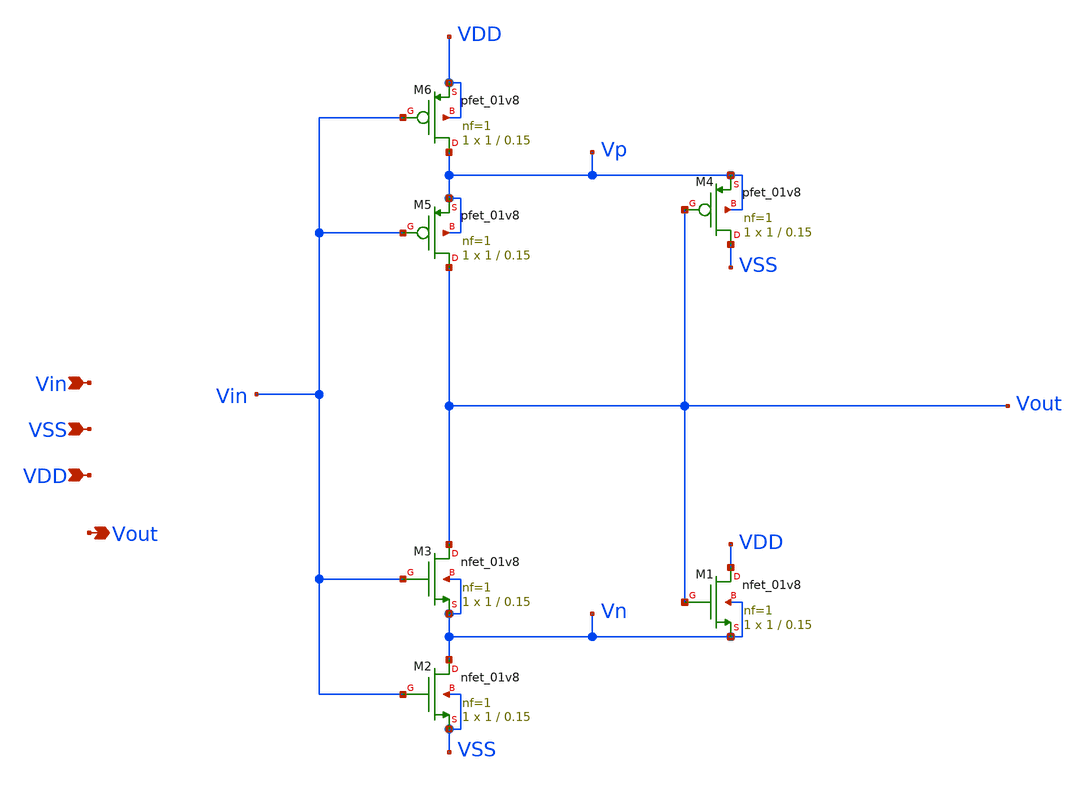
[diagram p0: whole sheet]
** sch_path: xschem/T1/schmTrigg/schmTrigg.sch
**.subckt schmTrigg Vin VDD VSS Vout
*.ipin Vin
*.ipin VDD
*.ipin VSS
*.opin Vout
XM1 VDD Vout Vn Vn sky130_fd_pr__nfet_01v8 L=0.15 W=1 nf=1 ad='int((1 + 1)/2) * 1 / 1 * 0.29' as='int((1 + 2)/2) * 1 / 1 * 0.29'
+ pd='2*int((1 + 1)/2) * (1 / 1 + 0.29)' ps='2*int((1 + 2)/2) * (1 / 1 + 0.29)' nrd='0.29 / 1 ' nrs='0.29 / 1 '
+ sa=0 sb=0 sd=0 mult=1 m=1
XM2 Vn Vin VSS VSS sky130_fd_pr__nfet_01v8 L=0.15 W=1 nf=1 ad='int((1 + 1)/2) * 1 / 1 * 0.29' as='int((1 + 2)/2) * 1 / 1 * 0.29'
+ pd='2*int((1 + 1)/2) * (1 / 1 + 0.29)' ps='2*int((1 + 2)/2) * (1 / 1 + 0.29)' nrd='0.29 / 1 ' nrs='0.29 / 1 '
+ sa=0 sb=0 sd=0 mult=1 m=1
XM3 Vout Vin Vn Vn sky130_fd_pr__nfet_01v8 L=0.15 W=1 nf=1 ad='int((1 + 1)/2) * 1 / 1 * 0.29' as='int((1 + 2)/2) * 1 / 1 * 0.29'
+ pd='2*int((1 + 1)/2) * (1 / 1 + 0.29)' ps='2*int((1 + 2)/2) * (1 / 1 + 0.29)' nrd='0.29 / 1 ' nrs='0.29 / 1 '
+ sa=0 sb=0 sd=0 mult=1 m=1
XM4 VSS Vout Vp Vp sky130_fd_pr__pfet_01v8 L=0.15 W=1 nf=1 ad='int((nf+1)/2) * W/nf * 0.29' as='int((nf+2)/2) * W/nf * 0.29'
+ pd='2*int((nf+1)/2) * (W/nf + 0.29)' ps='2*int((nf+2)/2) * (W/nf + 0.29)' nrd='0.29 / W' nrs='0.29 / W'
+ sa=0 sb=0 sd=0 mult=1 m=1
XM5 Vout Vin Vp Vp sky130_fd_pr__pfet_01v8 L=0.15 W=1 nf=1 ad='int((nf+1)/2) * W/nf * 0.29' as='int((nf+2)/2) * W/nf * 0.29'
+ pd='2*int((nf+1)/2) * (W/nf + 0.29)' ps='2*int((nf+2)/2) * (W/nf + 0.29)' nrd='0.29 / W' nrs='0.29 / W'
+ sa=0 sb=0 sd=0 mult=1 m=1
XM6 Vp Vin VDD VDD sky130_fd_pr__pfet_01v8 L=0.15 W=1 nf=1 ad='int((nf+1)/2) * W/nf * 0.29' as='int((nf+2)/2) * W/nf * 0.29'
+ pd='2*int((nf+1)/2) * (W/nf + 0.29)' ps='2*int((nf+2)/2) * (W/nf + 0.29)' nrd='0.29 / W' nrs='0.29 / W'
+ sa=0 sb=0 sd=0 mult=1 m=1
**.ends
.end
